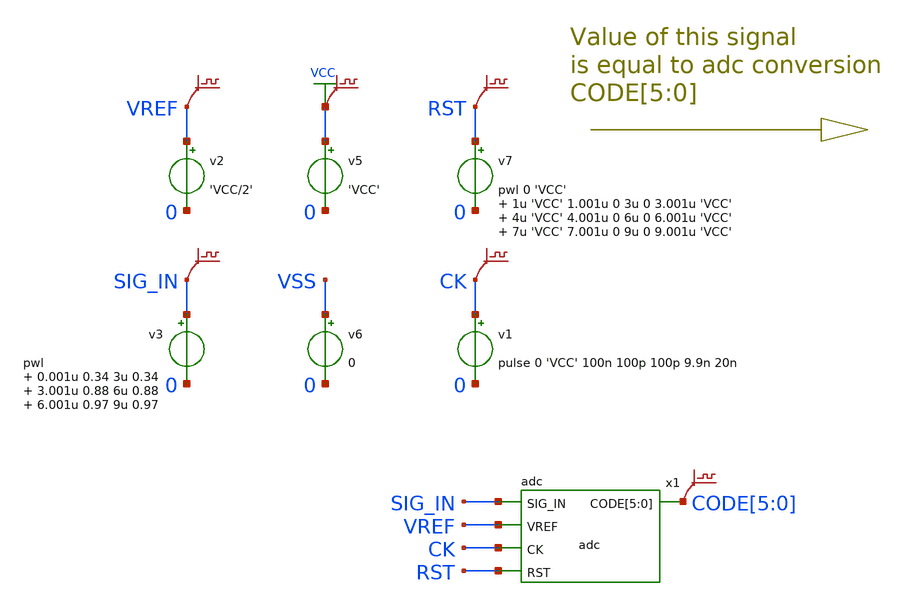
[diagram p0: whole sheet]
** sch_path: xschem_library_oa/ngspice/delta_sigma/schematic/delta_sigma.sch
* Copyright (C) 1998-2024 Stefan Frederik Schippers
* This program is free software; you can redistribute it and/or modify
* it under the terms of the GNU General Public License as published by
* the Free Software Foundation; either version 2 of the License, or
* (at your option) any later version.
* This program is distributed in the hope that it will be useful,
* but WITHOUT ANY WARRANTY; without even the implied warranty of
* MERCHANTABILITY or FITNESS FOR A PARTICULAR PURPOSE.  See the
* GNU General Public License for more details.
* You should have received a copy of the GNU General Public License
* along with this program; if not, write to the Free Software
**.subckt delta_sigma
v2 VREF 0 'VCC/2'
v3 SIG_IN 0 pwl 0.001u 0.34 3u 0.34 3.001u 0.88 6u 0.88 6.001u 0.97 9u 0.97
v1 CK 0 pulse 0 'VCC' 100n 100p 100p 9.9n 20n
v5 VCC 0 'VCC'
v6 VSS 0 0
v7 RST 0 pwl 0 'VCC' 1u 'VCC' 1.001u 0 3u 0 3.001u 'VCC' 4u 'VCC' 4.001u 0 6u 0 6.001u 'VCC' 7u 'VCC'
+ 7.001u 0 9u 0 9.001u 'VCC'
x1 CODE[5] CODE[4] CODE[3] CODE[2] CODE[1] CODE[0] SIG_IN VREF CK RST adc
.save v(vref)
.save v(vcc)
.save v(sig_in)
.save v(ck)
.save v(rst)
.save v(code[5])
.save v(code[4])
.save v(code[3])
.save v(code[2])
.save v(code[1])
.save v(code[0])
**** begin user architecture code



** download the models from:
** https://ptm.asu.edu/modelcard/65nm_bulk.txt
.include models_65nm.txt
.model switch sw vt='VCC/2' vh=0.2 ron=1000 roff=1G
.param VCC=1.2
.option method=GEAR
.measure tran avg1 AVG v(x1.qn) from=1u to=3u
.measure tran avg2 AVG v(x1.qn) from=4u to=6u
.measure tran avg3 AVG v(x1.qn) from=7u to=9u
.control
  tran 0.2n 9u uic
  write delta_sigma.raw
  set appendwrite
  save all
  op
  write delta_sigma.raw
  quit 0
.endc



**** end user architecture code
**.ends
.GLOBAL VCC
.end
